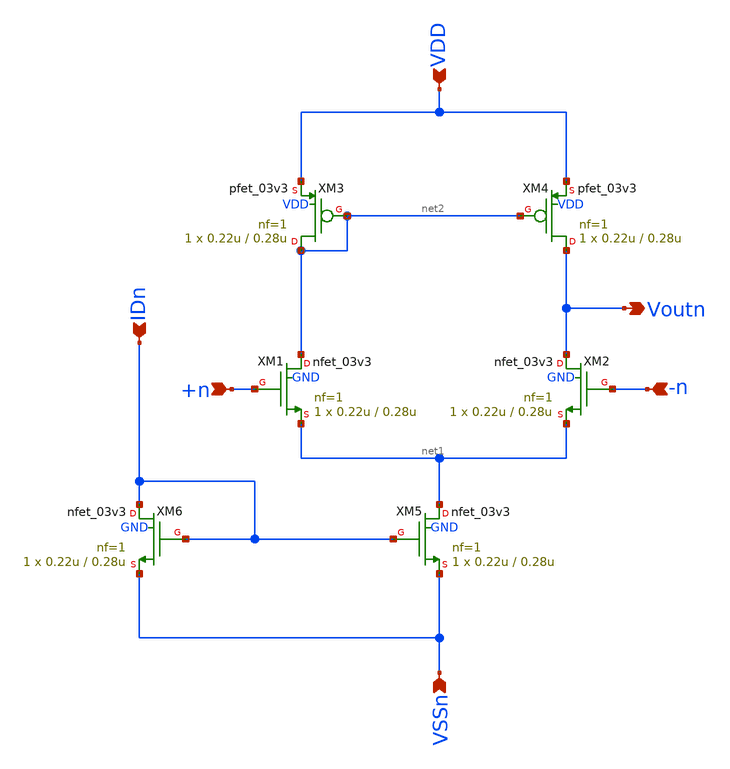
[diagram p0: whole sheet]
** sch_path: xschem/ota_miller/ota_n_in.sch
**.subckt ota_n_in Voutn VSSn VDD +n -n IDn
*.opin Voutn
*.ipin VSSn
*.ipin VDD
*.ipin +n
*.ipin -n
*.ipin IDn
XM1 net2 +n net1 GND nfet_03v3 L=0.28u W=0.22u nf=1 ad='int((nf+1)/2) * W/nf * 0.18u' as='int((nf+2)/2) * W/nf * 0.18u'
+ pd='2*int((nf+1)/2) * (W/nf + 0.18u)' ps='2*int((nf+2)/2) * (W/nf + 0.18u)' nrd='0.18u / W' nrs='0.18u / W'
+ sa=0 sb=0 sd=0 m=1 par=1
XM2 Voutn -n net1 GND nfet_03v3 L=0.28u W=0.22u nf=1 ad='int((nf+1)/2) * W/nf * 0.18u' as='int((nf+2)/2) * W/nf * 0.18u'
+ pd='2*int((nf+1)/2) * (W/nf + 0.18u)' ps='2*int((nf+2)/2) * (W/nf + 0.18u)' nrd='0.18u / W' nrs='0.18u / W'
+ sa=0 sb=0 sd=0 m=1 par=1
XM3 net2 net2 VDD VDD pfet_03v3 L=0.28u W=0.22u nf=1 ad='int((nf+1)/2) * W/nf * 0.18u' as='int((nf+2)/2) * W/nf * 0.18u'
+ pd='2*int((nf+1)/2) * (W/nf + 0.18u)' ps='2*int((nf+2)/2) * (W/nf + 0.18u)' nrd='0.18u / W' nrs='0.18u / W'
+ sa=0 sb=0 sd=0 m=1 par=1
XM4 Voutn net2 VDD VDD pfet_03v3 L=0.28u W=0.22u nf=1 ad='int((nf+1)/2) * W/nf * 0.18u' as='int((nf+2)/2) * W/nf * 0.18u'
+ pd='2*int((nf+1)/2) * (W/nf + 0.18u)' ps='2*int((nf+2)/2) * (W/nf + 0.18u)' nrd='0.18u / W' nrs='0.18u / W'
+ sa=0 sb=0 sd=0 m=1 par=1
XM5 net1 IDn VSSn GND nfet_03v3 L=0.28u W=0.22u nf=1 ad='int((nf+1)/2) * W/nf * 0.18u' as='int((nf+2)/2) * W/nf * 0.18u'
+ pd='2*int((nf+1)/2) * (W/nf + 0.18u)' ps='2*int((nf+2)/2) * (W/nf + 0.18u)' nrd='0.18u / W' nrs='0.18u / W'
+ sa=0 sb=0 sd=0 m=1 par=1
XM6 IDn IDn VSSn GND nfet_03v3 L=0.28u W=0.22u nf=1 ad='int((nf+1)/2) * W/nf * 0.18u' as='int((nf+2)/2) * W/nf * 0.18u'
+ pd='2*int((nf+1)/2) * (W/nf + 0.18u)' ps='2*int((nf+2)/2) * (W/nf + 0.18u)' nrd='0.18u / W' nrs='0.18u / W'
+ sa=0 sb=0 sd=0 m=1 par=1
**.ends
.end
